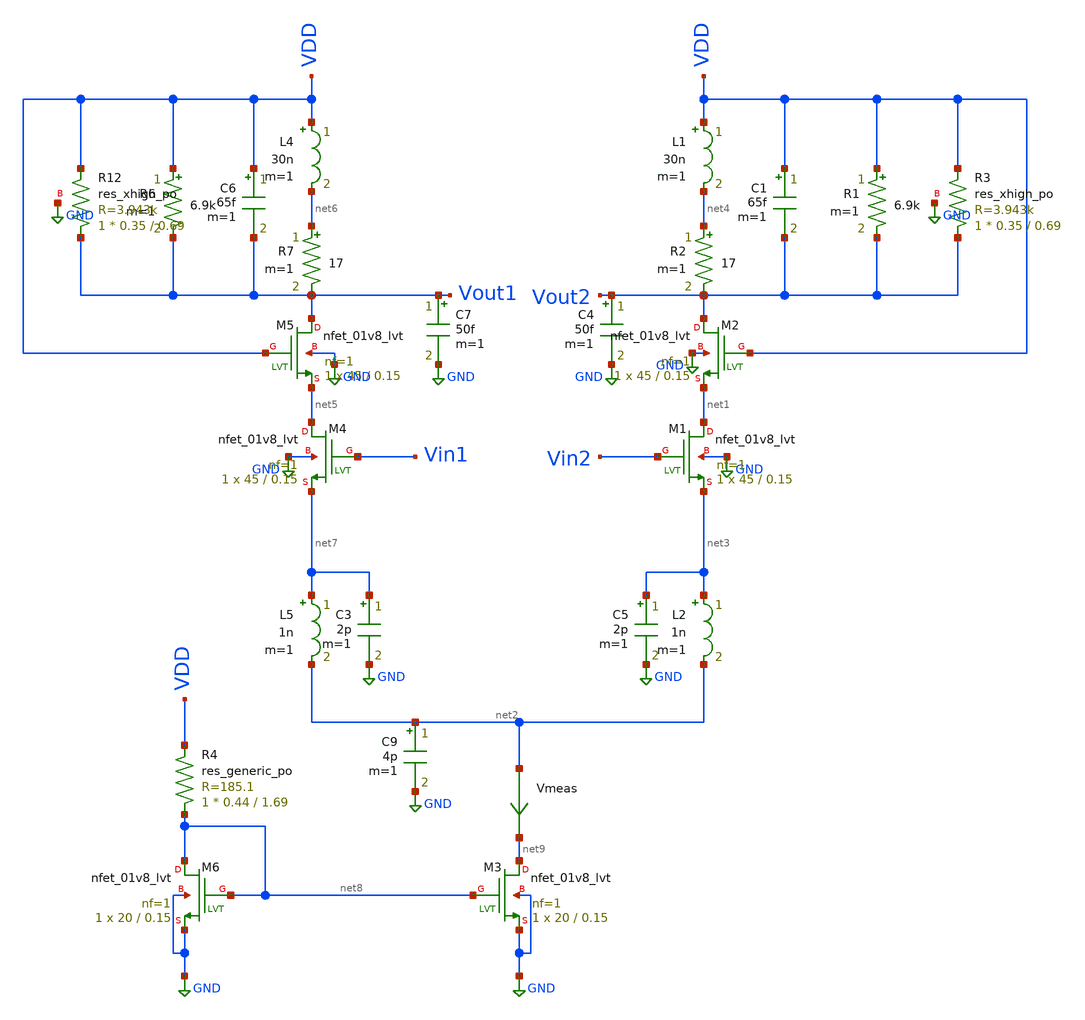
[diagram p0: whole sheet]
** sch_path: skywater_stuff/ECE631_RF_CMOS/untitled-6.sch
**.subckt untitled-6
XM1 net1 Vin2 net3 GND sky130_fd_pr__nfet_01v8_lvt L=0.15 W=45 nf=1 ad='int((nf+1)/2) * W/nf * 0.29'
+ as='int((nf+2)/2) * W/nf * 0.29' pd='2*int((nf+1)/2) * (W/nf + 0.29)' ps='2*int((nf+2)/2) * (W/nf + 0.29)'
+ nrd='0.29 / W' nrs='0.29 / W' sa=0 sb=0 sd=0 mult=1 m=1
L1 VDD net4 30n m=1
XM2 Vout2 VDD net1 GND sky130_fd_pr__nfet_01v8_lvt L=0.15 W=45 nf=1 ad='int((nf+1)/2) * W/nf * 0.29'
+ as='int((nf+2)/2) * W/nf * 0.29' pd='2*int((nf+1)/2) * (W/nf + 0.29)' ps='2*int((nf+2)/2) * (W/nf + 0.29)'
+ nrd='0.29 / W' nrs='0.29 / W' sa=0 sb=0 sd=0 mult=1 m=1
C1 VDD Vout2 65f m=1
L2 net3 net2 1n m=1
R1 VDD Vout2 6.9k m=1
R2 net4 Vout2 17 m=1
C4 Vout2 GND 50f m=1
XM4 net5 Vin1 net7 GND sky130_fd_pr__nfet_01v8_lvt L=0.15 W=45 nf=1 ad='int((nf+1)/2) * W/nf * 0.29'
+ as='int((nf+2)/2) * W/nf * 0.29' pd='2*int((nf+1)/2) * (W/nf + 0.29)' ps='2*int((nf+2)/2) * (W/nf + 0.29)'
+ nrd='0.29 / W' nrs='0.29 / W' sa=0 sb=0 sd=0 mult=1 m=1
L4 VDD net6 30n m=1
XM5 Vout1 VDD net5 GND sky130_fd_pr__nfet_01v8_lvt L=0.15 W=45 nf=1 ad='int((nf+1)/2) * W/nf * 0.29'
+ as='int((nf+2)/2) * W/nf * 0.29' pd='2*int((nf+1)/2) * (W/nf + 0.29)' ps='2*int((nf+2)/2) * (W/nf + 0.29)'
+ nrd='0.29 / W' nrs='0.29 / W' sa=0 sb=0 sd=0 mult=1 m=1
C6 VDD Vout1 65f m=1
R6 VDD Vout1 6.9k m=1
R7 net6 Vout1 17 m=1
C7 Vout1 GND 50f m=1
L5 net7 net2 1n m=1
XM3 net9 net8 GND GND sky130_fd_pr__nfet_01v8_lvt L=0.15 W=20 nf=1 ad='int((nf+1)/2) * W/nf * 0.29' as='int((nf+2)/2) * W/nf * 0.29'
+ pd='2*int((nf+1)/2) * (W/nf + 0.29)' ps='2*int((nf+2)/2) * (W/nf + 0.29)' nrd='0.29 / W' nrs='0.29 / W'
+ sa=0 sb=0 sd=0 mult=1 m=1
XM6 net8 net8 GND GND sky130_fd_pr__nfet_01v8_lvt L=0.15 W=20 nf=1 ad='int((nf+1)/2) * W/nf * 0.29' as='int((nf+2)/2) * W/nf * 0.29'
+ pd='2*int((nf+1)/2) * (W/nf + 0.29)' ps='2*int((nf+2)/2) * (W/nf + 0.29)' nrd='0.29 / W' nrs='0.29 / W'
+ sa=0 sb=0 sd=0 mult=1 m=1
Vmeas net2 net9 0
.save i(vmeas)
C3 net7 GND 2p m=1
C5 net3 GND 2p m=1
C9 net2 GND 4p m=1
XR12 Vout1 VDD GND sky130_fd_pr__res_xhigh_po W=0.35 L=0.69 mult=1 m=1
XR3 Vout2 VDD GND sky130_fd_pr__res_xhigh_po W=0.35 L=0.69 mult=1 m=1
XR4 net8 VDD sky130_fd_pr__res_generic_po W=0.44 L=1.69 m=1
**.ends
.GLOBAL GND
.end
